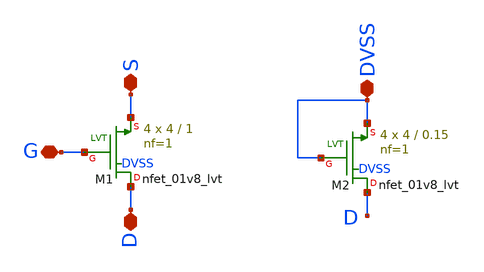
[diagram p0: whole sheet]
** sch_path: magic/trim.sch
**.subckt trim G D S DVSS
*.iopin G
*.iopin D
*.iopin S
*.iopin DVSS
XM1 D G S DVSS sky130_fd_pr__nfet_01v8_lvt L=1 W=4 nf=1 ad='int((nf+1)/2) * W/nf * 0.29' as='int((nf+2)/2) * W/nf * 0.29'
+ pd='2*int((nf+1)/2) * (W/nf + 0.29)' ps='2*int((nf+2)/2) * (W/nf + 0.29)' nrd='0.29 / W' nrs='0.29 / W'
+ sa=0 sb=0 sd=0 mult=4 m=4
XM2 D DVSS DVSS DVSS sky130_fd_pr__nfet_01v8_lvt L=0.15 W=4 nf=1 ad='int((nf+1)/2) * W/nf * 0.29' as='int((nf+2)/2) * W/nf * 0.29'
+ pd='2*int((nf+1)/2) * (W/nf + 0.29)' ps='2*int((nf+2)/2) * (W/nf + 0.29)' nrd='0.29 / W' nrs='0.29 / W'
+ sa=0 sb=0 sd=0 mult=4 m=4
**.ends
.end
